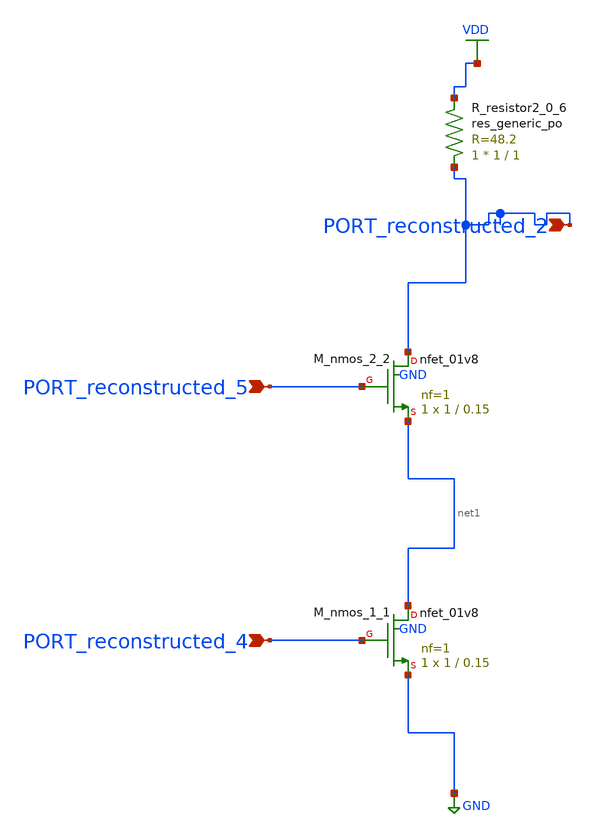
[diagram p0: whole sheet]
** sch_path: schematics/10_11591_ijece_v13i3_pp2618-2631_03_002.sch
**.subckt 10_11591_ijece_v13i3_pp2618-2631_03_002 PORT_reconstructed_5 PORT_reconstructed_4
*+ PORT_reconstructed_2
*.ipin PORT_reconstructed_5
*.ipin PORT_reconstructed_4
*.ipin PORT_reconstructed_2
XM_nmos_1_1 net1 PORT_reconstructed_4 GND GND sky130_fd_pr__nfet_01v8 L=0.15 W=1 nf=1 ad='int((1 + 1)/2) * 1 / 1 * 0.29'
+ as='int((1 + 2)/2) * 1 / 1 * 0.29' pd='2*int((1 + 1)/2) * (1 / 1 + 0.29)' ps='2*int((1 + 2)/2) * (1 / 1 + 0.29)'
+ nrd='0.29 / 1 ' nrs='0.29 / 1 ' sa=0 sb=0 sd=0 mult=1 m=1
XM_nmos_2_2 PORT_reconstructed_2 PORT_reconstructed_5 net1 GND sky130_fd_pr__nfet_01v8 L=0.15 W=1 nf=1
+ ad='int((1 + 1)/2) * 1 / 1 * 0.29' as='int((1 + 2)/2) * 1 / 1 * 0.29' pd='2*int((1 + 1)/2) * (1 / 1 + 0.29)'
+ ps='2*int((1 + 2)/2) * (1 / 1 + 0.29)' nrd='0.29 / 1 ' nrs='0.29 / 1 ' sa=0 sb=0 sd=0 mult=1 m=1
XR_resistor2_0_6 PORT_reconstructed_2 VDD sky130_fd_pr__res_generic_po W=1 L=1 m=1
**.ends
.GLOBAL GND
.GLOBAL VDD
.end
